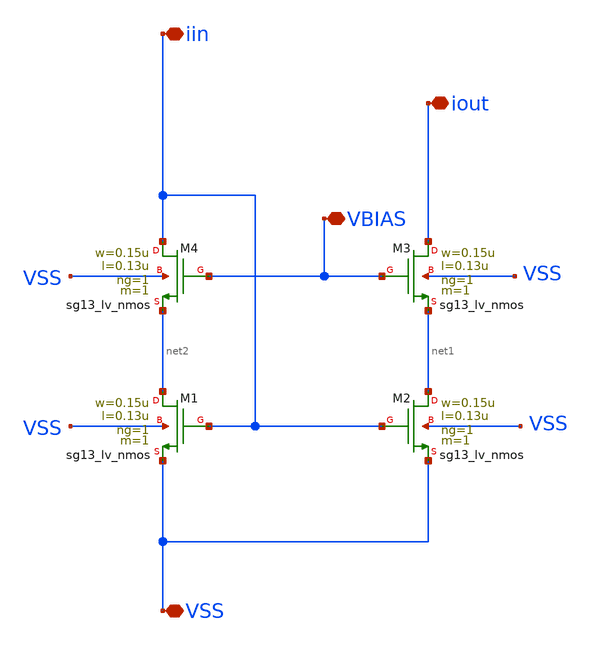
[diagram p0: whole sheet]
** sch_path: analog-db/templates/current_mirror/nmos_current_sink/low_voltage_cascode_current_mirror.sch
* Copyright 2026 MacAnalog Research Group
**.subckt low_voltage_cascode_current_mirror VSS iin iout VBIAS
*.iopin VSS
*.iopin iin
*.iopin iout
*.iopin VBIAS
XM1 net2 iin VSS VSS sg13_lv_nmos w=0.15u l=0.13u ng=1 m=1 mm_ok=1
XM2 net1 iin VSS VSS sg13_lv_nmos w=0.15u l=0.13u ng=1 m=1 mm_ok=1
XM3 iout VBIAS net1 VSS sg13_lv_nmos w=0.15u l=0.13u ng=1 m=1 mm_ok=1
XM4 iin VBIAS net2 VSS sg13_lv_nmos w=0.15u l=0.13u ng=1 m=1 mm_ok=1
**.ends
.end
